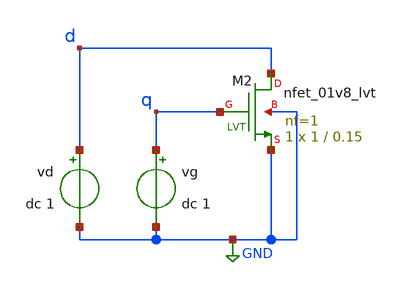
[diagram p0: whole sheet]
** sch_path: tb_cmos_characteristics.sch
**.subckt tb_cmos_characteristics
vg q GND dc 1
vd d GND dc 1
XM2 d q GND GND sky130_fd_pr__nfet_01v8_lvt L=0.15 W=1 nf=1 ad='int((nf+1)/2) * W/nf * 0.29' as='int((nf+2)/2) * W/nf * 0.29'
+ pd='2*int((nf+1)/2) * (W/nf + 0.29)' ps='2*int((nf+2)/2) * (W/nf + 0.29)' nrd='0.29 / W' nrs='0.29 / W'
+ sa=0 sb=0 sd=0 mult=1 m=1
**** begin user architecture code


* Circuit Parameters
.options TEMP = 27.0

* OP Parameters & Signal to save
*.save all  @m.x1.xm1.msky130_fd_pr__nfet_01v8[id]  @m.x1.xm1.msky130_fd_pr__nfet_01v8[vth]  @m.x1.xm1.msky130_fd_pr__nfet_01v8[vdsat]

* Control & Simulation
.save all

.control
*op
*print @m.x1.xm1.msky130_fd_pr__nfet_01v8[id]
*setplot op1
*write ~/xschem/simulation/tb_characteristics_op1.raw

reset
dc vd 0 3 0.01 vg 0.7 1 0.05
plot -i(vd)

* loop
*foreach var 10 20
*alterparam nmos ww = var
*op
*echo var: @m.x1.xm1.msky130_fd_pr__nfet_01v8[id]
*reset
*end
* end loop

.endc

.end



.include $::SKYWATER_MODELS/cells/nfet_01v8/sky130_fd_pr__nfet_01v8__tt.corner.spice
.include $::SKYWATER_MODELS/cells/nfet_01v8_lvt/sky130_fd_pr__nfet_01v8_lvt__tt.corner.spice
.include $::SKYWATER_MODELS/cells/pfet_01v8/sky130_fd_pr__pfet_01v8__tt.corner.spice
.include $::SKYWATER_MODELS/cells/nfet_03v3_nvt/sky130_fd_pr__nfet_03v3_nvt__tt.corner.spice
.include $::SKYWATER_MODELS/cells/nfet_05v0_nvt/sky130_fd_pr__nfet_05v0_nvt__tt.corner.spice
.include $::SKYWATER_MODELS/cells/esd_nfet_01v8/sky130_fd_pr__esd_nfet_01v8__tt.corner.spice
.include $::SKYWATER_MODELS/cells/pfet_01v8_lvt/sky130_fd_pr__pfet_01v8_lvt__tt.corner.spice
.include $::SKYWATER_MODELS/cells/pfet_01v8_hvt/sky130_fd_pr__pfet_01v8_hvt__tt.corner.spice
.include $::SKYWATER_MODELS/cells/esd_pfet_g5v0d10v5/sky130_fd_pr__esd_pfet_g5v0d10v5__tt.corner.spice
.include $::SKYWATER_MODELS/cells/pfet_g5v0d10v5/sky130_fd_pr__pfet_g5v0d10v5__tt.corner.spice
.include $::SKYWATER_MODELS/cells/pfet_g5v0d16v0/sky130_fd_pr__pfet_g5v0d16v0__tt.corner.spice
.include $::SKYWATER_MODELS/cells/nfet_g5v0d10v5/sky130_fd_pr__nfet_g5v0d10v5__tt.corner.spice
.include $::SKYWATER_MODELS/cells/nfet_g5v0d16v0/sky130_fd_pr__nfet_g5v0d16v0__tt_discrete.corner.spice
.include $::SKYWATER_MODELS/cells/esd_nfet_g5v0d10v5/sky130_fd_pr__esd_nfet_g5v0d10v5__tt.corner.spice
.include $::SKYWATER_MODELS/models/corners/tt/nonfet.spice
* Mismatch parameters
.include $::SKYWATER_MODELS/cells/nfet_01v8/sky130_fd_pr__nfet_01v8__mismatch.corner.spice
.include $::SKYWATER_MODELS/cells/pfet_01v8/sky130_fd_pr__pfet_01v8__mismatch.corner.spice
.include $::SKYWATER_MODELS/cells/nfet_01v8_lvt/sky130_fd_pr__nfet_01v8_lvt__mismatch.corner.spice
.include $::SKYWATER_MODELS/cells/pfet_01v8_lvt/sky130_fd_pr__pfet_01v8_lvt__mismatch.corner.spice
.include $::SKYWATER_MODELS/cells/pfet_01v8_hvt/sky130_fd_pr__pfet_01v8_hvt__mismatch.corner.spice
.include $::SKYWATER_MODELS/cells/nfet_g5v0d10v5/sky130_fd_pr__nfet_g5v0d10v5__mismatch.corner.spice
.include $::SKYWATER_MODELS/cells/pfet_g5v0d10v5/sky130_fd_pr__pfet_g5v0d10v5__mismatch.corner.spice
.include $::SKYWATER_MODELS/cells/nfet_05v0_nvt/sky130_fd_pr__nfet_05v0_nvt__mismatch.corner.spice
.include $::SKYWATER_MODELS/cells/nfet_03v3_nvt/sky130_fd_pr__nfet_03v3_nvt__mismatch.corner.spice
* Resistor$::SKYWATER_MODELS/Capacitor
.include $::SKYWATER_MODELS/models/r+c/res_typical__cap_typical.spice
.include $::SKYWATER_MODELS/models/r+c/res_typical__cap_typical__lin.spice
* Special cells
.include $::SKYWATER_MODELS/models/corners/tt/specialized_cells.spice
* All models
.include $::SKYWATER_MODELS/models/all.spice
* Corner
.include $::SKYWATER_MODELS/models/corners/tt/rf.spice

**** end user architecture code
**.ends
.GLOBAL GND
.end
